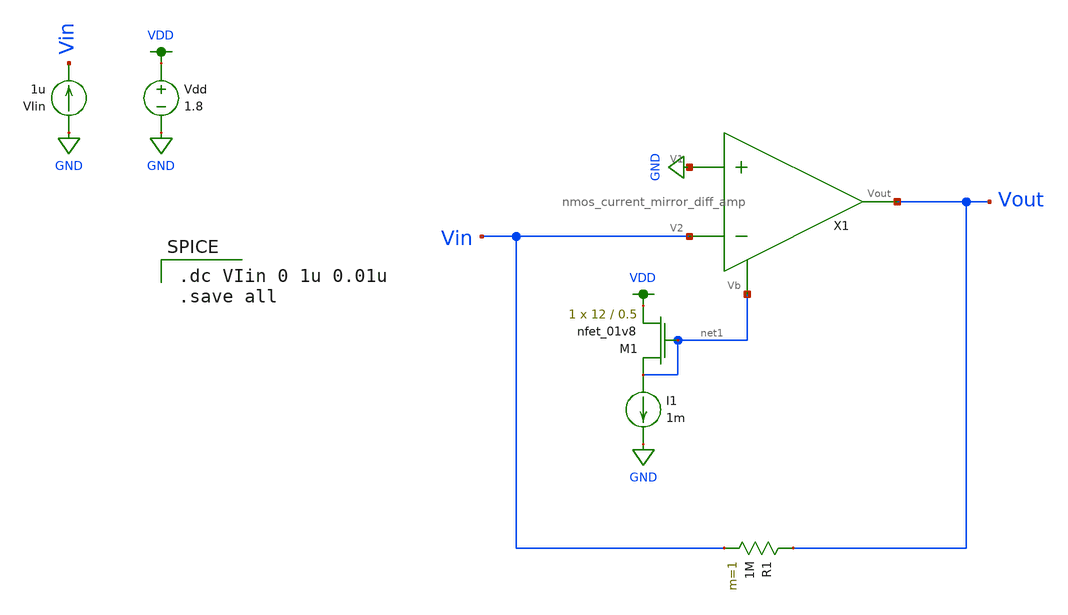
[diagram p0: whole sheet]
** sch_path: schematic/current-to-voltage.sch
**.subckt current-to-voltage
X1 net1 Vout GND Vin nmos_current_mirror_diff_amp
I1 net1 GND 1m
XM1 net1 net1 VDD GND sky130_fd_pr__nfet_01v8 L=0.5 W=12 nf=1 ad='int((nf+1)/2) * W/nf * 0.29' as='int((nf+2)/2) * W/nf * 0.29'
+ pd='2*int((nf+1)/2) * (W/nf + 0.29)' ps='2*int((nf+2)/2) * (W/nf + 0.29)' nrd='0.29 / W' nrs='0.29 / W'
+ sa=0 sb=0 sd=0 mult=1 m=1
Vdd VDD GND 1.8
VIin GND Vin 1u
R1 Vout Vin 1M m=1
**** begin user architecture code

.option wnflag=1
.param MC_SWITCH=0.0
.lib ~/skywater/skywater-pdk/libraries/sky130_fd_pr_ngspice/latest/models/sky130.lib.spice tt


.dc VIin 0 1u 0.01u
.save all

**** end user architecture code
**.ends

* expanding   symbol:
*+  /home/madvlsi/Documents/MADVLSI-Final_Project/schematic/nmos_current_mirror_diff_amp.sym # of pins=4
** sym_path: schematic/archive/nmos_current_mirror_diff_amp.sym
** sch_path: schematic/archive/nmos_current_mirror_diff_amp.sch
.subckt nmos_current_mirror_diff_amp Vb Vout V1 V2
*.ipin V1
*.ipin V2
*.ipin Vb
*.iopin Vout
XM1 net1 V1 net2 GND sky130_fd_pr__nfet_01v8 L=0.5 W=12 nf=1 ad='int((nf+1)/2) * W/nf * 0.29' as='int((nf+2)/2) * W/nf * 0.29'
+ pd='2*int((nf+1)/2) * (W/nf + 0.29)' ps='2*int((nf+2)/2) * (W/nf + 0.29)' nrd='0.29 / W' nrs='0.29 / W'
+ sa=0 sb=0 sd=0 mult=1 m=1
XM2 net2 V2 net3 GND sky130_fd_pr__nfet_01v8 L=0.5 W=12 nf=1 ad='int((nf+1)/2) * W/nf * 0.29' as='int((nf+2)/2) * W/nf * 0.29'
+ pd='2*int((nf+1)/2) * (W/nf + 0.29)' ps='2*int((nf+2)/2) * (W/nf + 0.29)' nrd='0.29 / W' nrs='0.29 / W'
+ sa=0 sb=0 sd=0 mult=1 m=1
XM3 net2 Vb GND GND sky130_fd_pr__nfet_01v8 L=0.5 W=12 nf=1 ad='int((nf+1)/2) * W/nf * 0.29' as='int((nf+2)/2) * W/nf * 0.29'
+ pd='2*int((nf+1)/2) * (W/nf + 0.29)' ps='2*int((nf+2)/2) * (W/nf + 0.29)' nrd='0.29 / W' nrs='0.29 / W'
+ sa=0 sb=0 sd=0 mult=1 m=1
XM4 GND net4 net4 GND sky130_fd_pr__nfet_01v8 L=0.5 W=12 nf=1 ad='int((nf+1)/2) * W/nf * 0.29' as='int((nf+2)/2) * W/nf * 0.29'
+ pd='2*int((nf+1)/2) * (W/nf + 0.29)' ps='2*int((nf+2)/2) * (W/nf + 0.29)' nrd='0.29 / W' nrs='0.29 / W'
+ sa=0 sb=0 sd=0 mult=1 m=1
XM5 Vout net4 GND GND sky130_fd_pr__nfet_01v8 L=0.5 W=12 nf=1 ad='int((nf+1)/2) * W/nf * 0.29' as='int((nf+2)/2) * W/nf * 0.29'
+ pd='2*int((nf+1)/2) * (W/nf + 0.29)' ps='2*int((nf+2)/2) * (W/nf + 0.29)' nrd='0.29 / W' nrs='0.29 / W'
+ sa=0 sb=0 sd=0 mult=1 m=1
XM6 VDD net1 net1 VDD sky130_fd_pr__pfet_01v8 L=0.5 W=12 nf=1 ad='int((nf+1)/2) * W/nf * 0.29' as='int((nf+2)/2) * W/nf * 0.29'
+ pd='2*int((nf+1)/2) * (W/nf + 0.29)' ps='2*int((nf+2)/2) * (W/nf + 0.29)' nrd='0.29 / W' nrs='0.29 / W'
+ sa=0 sb=0 sd=0 mult=1 m=1
XM7 VDD net3 net3 VDD sky130_fd_pr__pfet_01v8 L=0.5 W=12 nf=1 ad='int((nf+1)/2) * W/nf * 0.29' as='int((nf+2)/2) * W/nf * 0.29'
+ pd='2*int((nf+1)/2) * (W/nf + 0.29)' ps='2*int((nf+2)/2) * (W/nf + 0.29)' nrd='0.29 / W' nrs='0.29 / W'
+ sa=0 sb=0 sd=0 mult=1 m=1
XM8 net4 net3 VDD VDD sky130_fd_pr__pfet_01v8 L=0.5 W=12 nf=1 ad='int((nf+1)/2) * W/nf * 0.29' as='int((nf+2)/2) * W/nf * 0.29'
+ pd='2*int((nf+1)/2) * (W/nf + 0.29)' ps='2*int((nf+2)/2) * (W/nf + 0.29)' nrd='0.29 / W' nrs='0.29 / W'
+ sa=0 sb=0 sd=0 mult=1 m=1
XM9 Vout net1 VDD VDD sky130_fd_pr__pfet_01v8 L=0.5 W=12 nf=1 ad='int((nf+1)/2) * W/nf * 0.29' as='int((nf+2)/2) * W/nf * 0.29'
+ pd='2*int((nf+1)/2) * (W/nf + 0.29)' ps='2*int((nf+2)/2) * (W/nf + 0.29)' nrd='0.29 / W' nrs='0.29 / W'
+ sa=0 sb=0 sd=0 mult=1 m=1
.ends

.GLOBAL GND
.GLOBAL VDD
.end
